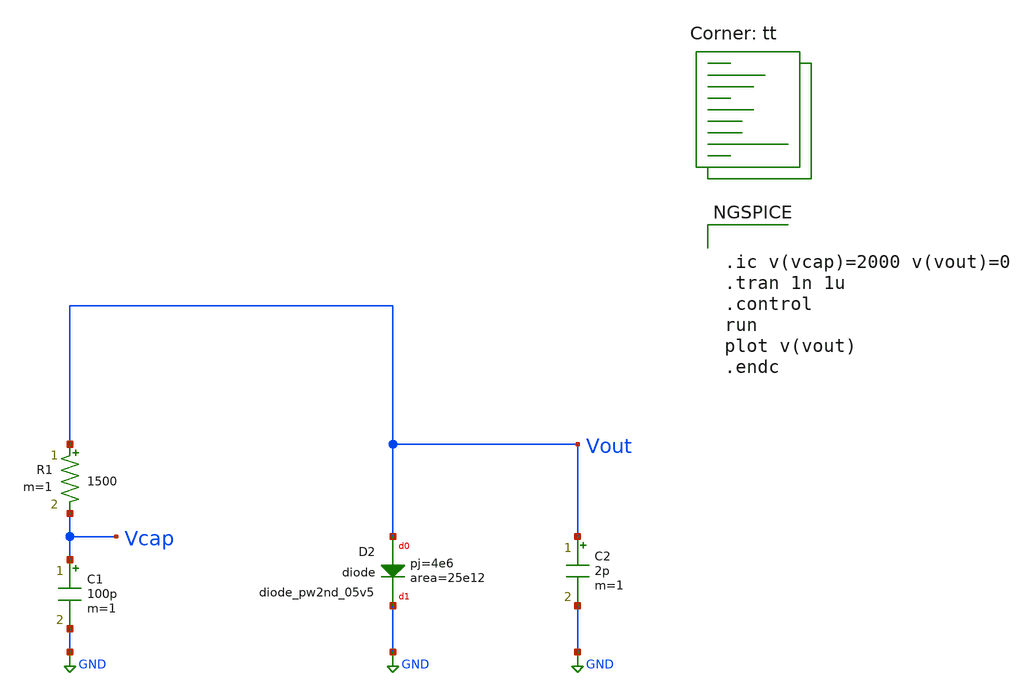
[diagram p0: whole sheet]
** sch_path: xschem/untitled.sch
**.subckt untitled
C1 Vcap GND 100p m=1
R1 Vout Vcap 1500 m=1
XD2 Vout GND sky130_fd_pr__diode_pw2nd_05v5 area=25e12 pj=4e6
C2 Vout GND 2p m=1
**** begin user architecture code


.ic v(vcap)=2000 v(vout)=0
.tran 1n 1u
.control
run
plot v(vout)
.endc


.lib $::SKYWATER_MODELS/sky130.lib.spice tt
**** end user architecture code
**.ends
.GLOBAL GND
.end
